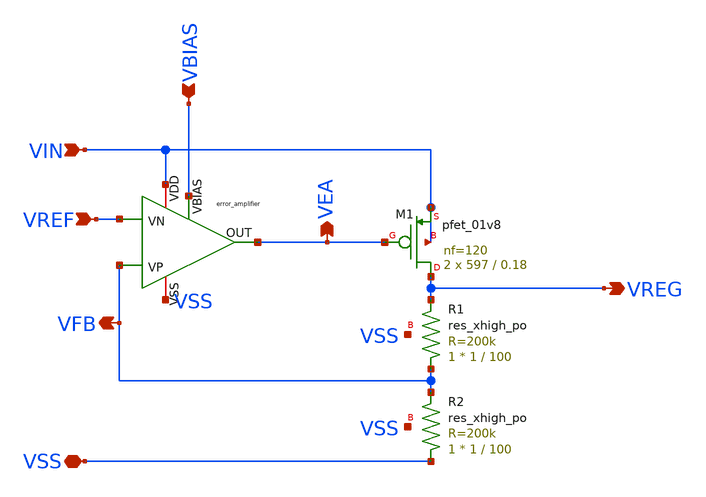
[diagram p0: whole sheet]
** sch_path: LDO_UVLO_Design/schematics/full_LDO_top.sch
**.subckt full_LDO_top VREF VSS VIN VBIAS VEA VREG VFB
*.ipin VREF
*.iopin VSS
*.ipin VIN
*.ipin VBIAS
*.opin VEA
*.opin VREG
*.opin VFB
x1 VIN VBIAS VFB VREF VEA VSS error_amplifier
XM1 VREG VEA VIN VIN sky130_fd_pr__pfet_01v8 L=0.18 W=597 nf=120 ad='int((nf+1)/2) * W/nf * 0.29' as='int((nf+2)/2) * W/nf * 0.29'
+ pd='2*int((nf+1)/2) * (W/nf + 0.29)' ps='2*int((nf+2)/2) * (W/nf + 0.29)' nrd='0.29 / W' nrs='0.29 / W'
+ sa=0 sb=0 sd=0 mult=2 m=2
XR1 VFB VREG VSS sky130_fd_pr__res_xhigh_po W=1 L=100 mult=1 m=1
XR2 VSS VFB VSS sky130_fd_pr__res_xhigh_po W=1 L=100 mult=1 m=1
**.ends

* expanding   symbol:  ldo-sky130A-its/LDO_UVLO_Design/schematics/error_amplifier.sym # of pins=6
** sym_path: LDO_UVLO_Design/schematics/error_amplifier.sym
** sch_path: LDO_UVLO_Design/schematics/error_amplifier.sch
.subckt error_amplifier VDD VBIAS VP VN OUT VSS
*.iopin VDD
*.iopin VSS
*.ipin VBIAS
*.ipin VP
*.ipin VN
*.opin OUT
XM1 net2 net2 VSS VSS sky130_fd_pr__nfet_01v8 L=1.5 W=12 nf=1 ad='int((nf+1)/2) * W/nf * 0.29' as='int((nf+2)/2) * W/nf * 0.29'
+ pd='2*int((nf+1)/2) * (W/nf + 0.29)' ps='2*int((nf+2)/2) * (W/nf + 0.29)' nrd='0.29 / W' nrs='0.29 / W'
+ sa=0 sb=0 sd=0 mult=1 m=1
XM2 net1 net1 VSS VSS sky130_fd_pr__nfet_01v8 L=1.5 W=12 nf=1 ad='int((nf+1)/2) * W/nf * 0.29' as='int((nf+2)/2) * W/nf * 0.29'
+ pd='2*int((nf+1)/2) * (W/nf + 0.29)' ps='2*int((nf+2)/2) * (W/nf + 0.29)' nrd='0.29 / W' nrs='0.29 / W'
+ sa=0 sb=0 sd=0 mult=1 m=1
XM3 net2 VP net4 VDD sky130_fd_pr__pfet_01v8 L=1.5 W=12 nf=1 ad='int((nf+1)/2) * W/nf * 0.29' as='int((nf+2)/2) * W/nf * 0.29'
+ pd='2*int((nf+1)/2) * (W/nf + 0.29)' ps='2*int((nf+2)/2) * (W/nf + 0.29)' nrd='0.29 / W' nrs='0.29 / W'
+ sa=0 sb=0 sd=0 mult=1 m=1
XM4 net1 VN net4 VDD sky130_fd_pr__pfet_01v8 L=1.5 W=12 nf=1 ad='int((nf+1)/2) * W/nf * 0.29' as='int((nf+2)/2) * W/nf * 0.29'
+ pd='2*int((nf+1)/2) * (W/nf + 0.29)' ps='2*int((nf+2)/2) * (W/nf + 0.29)' nrd='0.29 / W' nrs='0.29 / W'
+ sa=0 sb=0 sd=0 mult=1 m=1
XM7 net3 net1 VSS VSS sky130_fd_pr__nfet_01v8 L=1.5 W=12 nf=1 ad='int((nf+1)/2) * W/nf * 0.29' as='int((nf+2)/2) * W/nf * 0.29'
+ pd='2*int((nf+1)/2) * (W/nf + 0.29)' ps='2*int((nf+2)/2) * (W/nf + 0.29)' nrd='0.29 / W' nrs='0.29 / W'
+ sa=0 sb=0 sd=0 mult=1 m=1
XM8 OUT net2 VSS VSS sky130_fd_pr__nfet_01v8 L=1.5 W=12 nf=1 ad='int((nf+1)/2) * W/nf * 0.29' as='int((nf+2)/2) * W/nf * 0.29'
+ pd='2*int((nf+1)/2) * (W/nf + 0.29)' ps='2*int((nf+2)/2) * (W/nf + 0.29)' nrd='0.29 / W' nrs='0.29 / W'
+ sa=0 sb=0 sd=0 mult=1 m=1
XM9 net3 net3 VDD VDD sky130_fd_pr__pfet_01v8 L=1.5 W=12 nf=1 ad='int((nf+1)/2) * W/nf * 0.29' as='int((nf+2)/2) * W/nf * 0.29'
+ pd='2*int((nf+1)/2) * (W/nf + 0.29)' ps='2*int((nf+2)/2) * (W/nf + 0.29)' nrd='0.29 / W' nrs='0.29 / W'
+ sa=0 sb=0 sd=0 mult=1 m=1
XM10 OUT net3 VDD VDD sky130_fd_pr__pfet_01v8 L=1.5 W=12 nf=1 ad='int((nf+1)/2) * W/nf * 0.29' as='int((nf+2)/2) * W/nf * 0.29'
+ pd='2*int((nf+1)/2) * (W/nf + 0.29)' ps='2*int((nf+2)/2) * (W/nf + 0.29)' nrd='0.29 / W' nrs='0.29 / W'
+ sa=0 sb=0 sd=0 mult=1 m=1
XM11 net4 VBIAS VDD VDD sky130_fd_pr__pfet_01v8 L=1.5 W=12 nf=1 ad='int((nf+1)/2) * W/nf * 0.29' as='int((nf+2)/2) * W/nf * 0.29'
+ pd='2*int((nf+1)/2) * (W/nf + 0.29)' ps='2*int((nf+2)/2) * (W/nf + 0.29)' nrd='0.29 / W' nrs='0.29 / W'
+ sa=0 sb=0 sd=0 mult=1 m=1
.ends

.end
